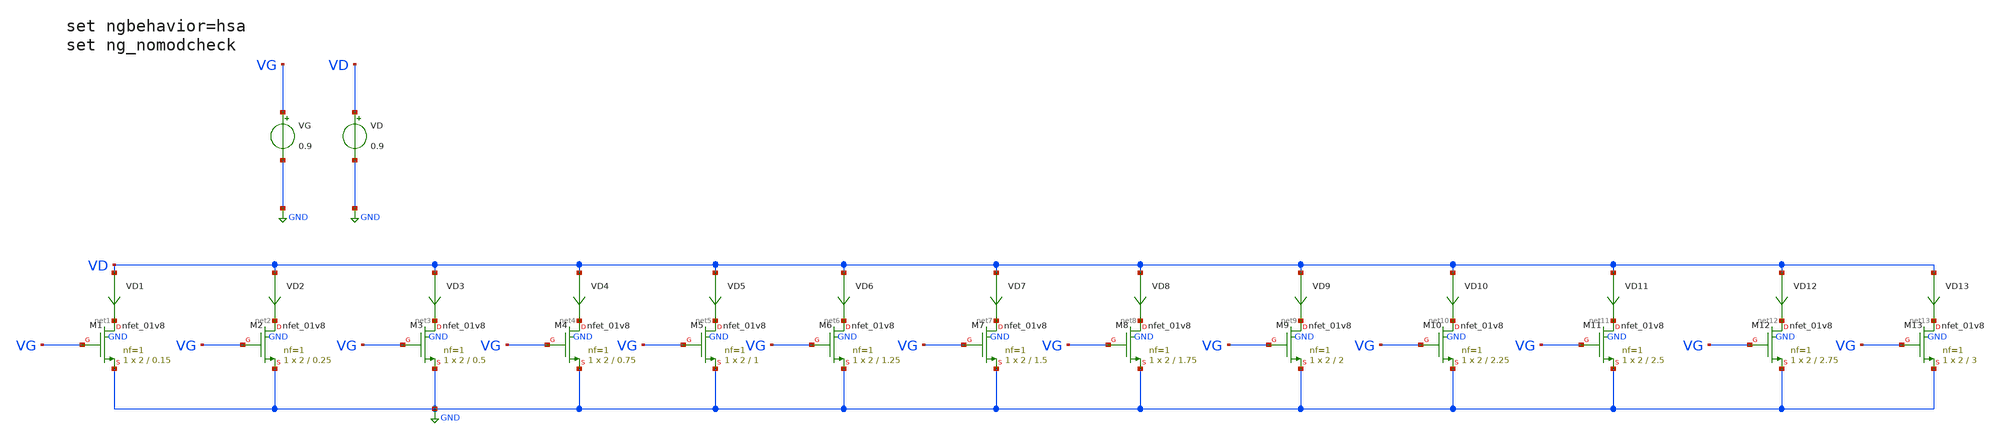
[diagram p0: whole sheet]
** sch_path: Design-Files/gmid_nmos_1v8_svt_tb.sch
**.subckt gmid_nmos_1v8_svt_tb
VG VG GND 0.9
VD VD GND 0.9
VD1 VD net1 0
.save i(vd1)
VD2 VD net2 0
.save i(vd2)
VD3 VD net3 0
.save i(vd3)
VD4 VD net4 0
.save i(vd4)
VD5 VD net5 0
.save i(vd5)
VD6 VD net6 0
.save i(vd6)
VD7 VD net7 0
.save i(vd7)
VD8 VD net8 0
.save i(vd8)
VD9 VD net9 0
.save i(vd9)
VD10 VD net10 0
.save i(vd10)
VD11 VD net11 0
.save i(vd11)
VD12 VD net12 0
.save i(vd12)
VD13 VD net13 0
.save i(vd13)
XM1 net1 VG GND GND sky130_fd_pr__nfet_01v8 L=0.15 W=2 nf=1 ad='int((nf+1)/2) * W/nf * 0.29' as='int((nf+2)/2) * W/nf * 0.29'
+ pd='2*int((nf+1)/2) * (W/nf + 0.29)' ps='2*int((nf+2)/2) * (W/nf + 0.29)' nrd='0.29 / W' nrs='0.29 / W'
+ sa=0 sb=0 sd=0 mult=1 m=1
XM2 net2 VG GND GND sky130_fd_pr__nfet_01v8 L=0.25 W=2 nf=1 ad='int((nf+1)/2) * W/nf * 0.29' as='int((nf+2)/2) * W/nf * 0.29'
+ pd='2*int((nf+1)/2) * (W/nf + 0.29)' ps='2*int((nf+2)/2) * (W/nf + 0.29)' nrd='0.29 / W' nrs='0.29 / W'
+ sa=0 sb=0 sd=0 mult=1 m=1
XM3 net3 VG GND GND sky130_fd_pr__nfet_01v8 L=0.5 W=2 nf=1 ad='int((nf+1)/2) * W/nf * 0.29' as='int((nf+2)/2) * W/nf * 0.29'
+ pd='2*int((nf+1)/2) * (W/nf + 0.29)' ps='2*int((nf+2)/2) * (W/nf + 0.29)' nrd='0.29 / W' nrs='0.29 / W'
+ sa=0 sb=0 sd=0 mult=1 m=1
XM4 net4 VG GND GND sky130_fd_pr__nfet_01v8 L=0.75 W=2 nf=1 ad='int((nf+1)/2) * W/nf * 0.29' as='int((nf+2)/2) * W/nf * 0.29'
+ pd='2*int((nf+1)/2) * (W/nf + 0.29)' ps='2*int((nf+2)/2) * (W/nf + 0.29)' nrd='0.29 / W' nrs='0.29 / W'
+ sa=0 sb=0 sd=0 mult=1 m=1
XM5 net5 VG GND GND sky130_fd_pr__nfet_01v8 L=1 W=2 nf=1 ad='int((nf+1)/2) * W/nf * 0.29' as='int((nf+2)/2) * W/nf * 0.29'
+ pd='2*int((nf+1)/2) * (W/nf + 0.29)' ps='2*int((nf+2)/2) * (W/nf + 0.29)' nrd='0.29 / W' nrs='0.29 / W'
+ sa=0 sb=0 sd=0 mult=1 m=1
XM6 net6 VG GND GND sky130_fd_pr__nfet_01v8 L=1.25 W=2 nf=1 ad='int((nf+1)/2) * W/nf * 0.29' as='int((nf+2)/2) * W/nf * 0.29'
+ pd='2*int((nf+1)/2) * (W/nf + 0.29)' ps='2*int((nf+2)/2) * (W/nf + 0.29)' nrd='0.29 / W' nrs='0.29 / W'
+ sa=0 sb=0 sd=0 mult=1 m=1
XM7 net7 VG GND GND sky130_fd_pr__nfet_01v8 L=1.5 W=2 nf=1 ad='int((nf+1)/2) * W/nf * 0.29' as='int((nf+2)/2) * W/nf * 0.29'
+ pd='2*int((nf+1)/2) * (W/nf + 0.29)' ps='2*int((nf+2)/2) * (W/nf + 0.29)' nrd='0.29 / W' nrs='0.29 / W'
+ sa=0 sb=0 sd=0 mult=1 m=1
XM8 net8 VG GND GND sky130_fd_pr__nfet_01v8 L=1.75 W=2 nf=1 ad='int((nf+1)/2) * W/nf * 0.29' as='int((nf+2)/2) * W/nf * 0.29'
+ pd='2*int((nf+1)/2) * (W/nf + 0.29)' ps='2*int((nf+2)/2) * (W/nf + 0.29)' nrd='0.29 / W' nrs='0.29 / W'
+ sa=0 sb=0 sd=0 mult=1 m=1
XM9 net9 VG GND GND sky130_fd_pr__nfet_01v8 L=2 W=2 nf=1 ad='int((nf+1)/2) * W/nf * 0.29' as='int((nf+2)/2) * W/nf * 0.29'
+ pd='2*int((nf+1)/2) * (W/nf + 0.29)' ps='2*int((nf+2)/2) * (W/nf + 0.29)' nrd='0.29 / W' nrs='0.29 / W'
+ sa=0 sb=0 sd=0 mult=1 m=1
XM10 net10 VG GND GND sky130_fd_pr__nfet_01v8 L=2.25 W=2 nf=1 ad='int((nf+1)/2) * W/nf * 0.29' as='int((nf+2)/2) * W/nf * 0.29'
+ pd='2*int((nf+1)/2) * (W/nf + 0.29)' ps='2*int((nf+2)/2) * (W/nf + 0.29)' nrd='0.29 / W' nrs='0.29 / W'
+ sa=0 sb=0 sd=0 mult=1 m=1
XM11 net11 VG GND GND sky130_fd_pr__nfet_01v8 L=2.5 W=2 nf=1 ad='int((nf+1)/2) * W/nf * 0.29' as='int((nf+2)/2) * W/nf * 0.29'
+ pd='2*int((nf+1)/2) * (W/nf + 0.29)' ps='2*int((nf+2)/2) * (W/nf + 0.29)' nrd='0.29 / W' nrs='0.29 / W'
+ sa=0 sb=0 sd=0 mult=1 m=1
XM12 net12 VG GND GND sky130_fd_pr__nfet_01v8 L=2.75 W=2 nf=1 ad='int((nf+1)/2) * W/nf * 0.29' as='int((nf+2)/2) * W/nf * 0.29'
+ pd='2*int((nf+1)/2) * (W/nf + 0.29)' ps='2*int((nf+2)/2) * (W/nf + 0.29)' nrd='0.29 / W' nrs='0.29 / W'
+ sa=0 sb=0 sd=0 mult=1 m=1
XM13 net13 VG GND GND sky130_fd_pr__nfet_01v8 L=3 W=2 nf=1 ad='int((nf+1)/2) * W/nf * 0.29' as='int((nf+2)/2) * W/nf * 0.29'
+ pd='2*int((nf+1)/2) * (W/nf + 0.29)' ps='2*int((nf+2)/2) * (W/nf + 0.29)' nrd='0.29 / W' nrs='0.29 / W'
+ sa=0 sb=0 sd=0 mult=1 m=1
**** begin user architecture code

** opencircuitdesign pdks install
.lib $::SKYWATER_MODELS/sky130.lib.spice ff



* ngspice commands
.option wnflag=1
.option savecurrents
.control
save all
save @m.xm1.msky130_fd_pr__nfet_01v8[gm]
save @m.xm1.msky130_fd_pr__nfet_01v8[vth]
save @m.xm1.msky130_fd_pr__nfet_01v8[gds]
save @m.xm1.msky130_fd_pr__nfet_01v8[cgg]
save @m.xm1.msky130_fd_pr__nfet_01v8[cgs]
save @m.xm1.msky130_fd_pr__nfet_01v8[cgd]
save @m.xm2.msky130_fd_pr__nfet_01v8[gm]
save @m.xm2.msky130_fd_pr__nfet_01v8[vth]
save @m.xm2.msky130_fd_pr__nfet_01v8[gds]
save @m.xm2.msky130_fd_pr__nfet_01v8[cgg]
save @m.xm2.msky130_fd_pr__nfet_01v8[cgs]
save @m.xm2.msky130_fd_pr__nfet_01v8[cgd]
save @m.xm3.msky130_fd_pr__nfet_01v8[gm]
save @m.xm3.msky130_fd_pr__nfet_01v8[vth]
save @m.xm3.msky130_fd_pr__nfet_01v8[gds]
save @m.xm3.msky130_fd_pr__nfet_01v8[cgg]
save @m.xm3.msky130_fd_pr__nfet_01v8[cgs]
save @m.xm3.msky130_fd_pr__nfet_01v8[cgd]
save @m.xm4.msky130_fd_pr__nfet_01v8[gm]
save @m.xm4.msky130_fd_pr__nfet_01v8[vth]
save @m.xm4.msky130_fd_pr__nfet_01v8[gds]
save @m.xm4.msky130_fd_pr__nfet_01v8[cgg]
save @m.xm4.msky130_fd_pr__nfet_01v8[cgs]
save @m.xm4.msky130_fd_pr__nfet_01v8[cgd]
save @m.xm5.msky130_fd_pr__nfet_01v8[gm]
save @m.xm5.msky130_fd_pr__nfet_01v8[vth]
save @m.xm5.msky130_fd_pr__nfet_01v8[gds]
save @m.xm5.msky130_fd_pr__nfet_01v8[cgg]
save @m.xm5.msky130_fd_pr__nfet_01v8[cgs]
save @m.xm5.msky130_fd_pr__nfet_01v8[cgd]
save @m.xm6.msky130_fd_pr__nfet_01v8[gm]
save @m.xm6.msky130_fd_pr__nfet_01v8[vth]
save @m.xm6.msky130_fd_pr__nfet_01v8[gds]
save @m.xm6.msky130_fd_pr__nfet_01v8[cgg]
save @m.xm6.msky130_fd_pr__nfet_01v8[cgs]
save @m.xm6.msky130_fd_pr__nfet_01v8[cgd]
save @m.xm7.msky130_fd_pr__nfet_01v8[gm]
save @m.xm7.msky130_fd_pr__nfet_01v8[vth]
save @m.xm7.msky130_fd_pr__nfet_01v8[gds]
save @m.xm7.msky130_fd_pr__nfet_01v8[cgg]
save @m.xm7.msky130_fd_pr__nfet_01v8[cgs]
save @m.xm7.msky130_fd_pr__nfet_01v8[cgd]
save @m.xm8.msky130_fd_pr__nfet_01v8[gm]
save @m.xm8.msky130_fd_pr__nfet_01v8[vth]
save @m.xm8.msky130_fd_pr__nfet_01v8[gds]
save @m.xm8.msky130_fd_pr__nfet_01v8[cgg]
save @m.xm8.msky130_fd_pr__nfet_01v8[cgs]
save @m.xm8.msky130_fd_pr__nfet_01v8[cgd]
save @m.xm9.msky130_fd_pr__nfet_01v8[gm]
save @m.xm9.msky130_fd_pr__nfet_01v8[vth]
save @m.xm9.msky130_fd_pr__nfet_01v8[gds]
save @m.xm9.msky130_fd_pr__nfet_01v8[cgg]
save @m.xm9.msky130_fd_pr__nfet_01v8[cgs]
save @m.xm9.msky130_fd_pr__nfet_01v8[cgd]
save @m.xm10.msky130_fd_pr__nfet_01v8[gm]
save @m.xm10.msky130_fd_pr__nfet_01v8[vth]
save @m.xm10.msky130_fd_pr__nfet_01v8[gds]
save @m.xm10.msky130_fd_pr__nfet_01v8[cgg]
save @m.xm10.msky130_fd_pr__nfet_01v8[cgs]
save @m.xm10.msky130_fd_pr__nfet_01v8[cgd]
save @m.xm11.msky130_fd_pr__nfet_01v8[gm]
save @m.xm11.msky130_fd_pr__nfet_01v8[vth]
save @m.xm11.msky130_fd_pr__nfet_01v8[gds]
save @m.xm11.msky130_fd_pr__nfet_01v8[cgg]
save @m.xm11.msky130_fd_pr__nfet_01v8[cgs]
save @m.xm11.msky130_fd_pr__nfet_01v8[cgd]
save @m.xm12.msky130_fd_pr__nfet_01v8[gm]
save @m.xm12.msky130_fd_pr__nfet_01v8[vth]
save @m.xm12.msky130_fd_pr__nfet_01v8[gds]
save @m.xm12.msky130_fd_pr__nfet_01v8[cgg]
save @m.xm12.msky130_fd_pr__nfet_01v8[cgs]
save @m.xm12.msky130_fd_pr__nfet_01v8[cgd]
save @m.xm13.msky130_fd_pr__nfet_01v8[gm]
save @m.xm13.msky130_fd_pr__nfet_01v8[vth]
save @m.xm13.msky130_fd_pr__nfet_01v8[gds]
save @m.xm13.msky130_fd_pr__nfet_01v8[cgg]
save @m.xm13.msky130_fd_pr__nfet_01v8[cgs]
save @m.xm13.msky130_fd_pr__nfet_01v8[cgd]
dc VG 0.05 1.8 0.1m
** remove zero length vectors to prevent write errors
remzerovec
write /foss/designs/PDKCHAR/gmid_nmos_svt_tb.raw

plot @m.xm1.msky130_fd_pr__nfet_01v8[gm]
plot @m.xm2.msky130_fd_pr__nfet_01v8[gm]
plot @m.xm3.msky130_fd_pr__nfet_01v8[gm]
plot @m.xm4.msky130_fd_pr__nfet_01v8[gm]
plot @m.xm5.msky130_fd_pr__nfet_01v8[gm]
plot @m.xm6.msky130_fd_pr__nfet_01v8[gm]
plot @m.xm7.msky130_fd_pr__nfet_01v8[gm]
plot @m.xm8.msky130_fd_pr__nfet_01v8[gm]
plot @m.xm9.msky130_fd_pr__nfet_01v8[gm]
plot @m.xm10.msky130_fd_pr__nfet_01v8[gm]
plot @m.xm11.msky130_fd_pr__nfet_01v8[gm]
plot @m.xm12.msky130_fd_pr__nfet_01v8[gm]
plot @m.xm13.msky130_fd_pr__nfet_01v8[gm]

wrdata /foss/designs/PDKCHAR/gmid_nmos_1_nfet_01v8_svt_tb.txt @m.xm1.msky130_fd_pr__nfet_01v8[gm]
+ i(VD1) @m.xm1.msky130_fd_pr__nfet_01v8[vth] @m.xm1.msky130_fd_pr__nfet_01v8[gds]
+ @m.xm1.msky130_fd_pr__nfet_01v8[cgg] @m.xm1.msky130_fd_pr__nfet_01v8[cgs] @m.xm1.msky130_fd_pr__nfet_01v8[cgd]
wrdata /foss/designs/PDKCHAR/gmid_nmos_2_nfet_01v8_svt_tb.txt @m.xm2.msky130_fd_pr__nfet_01v8[gm]
+ i(VD2) @m.xm2.msky130_fd_pr__nfet_01v8[vth] @m.xm2.msky130_fd_pr__nfet_01v8[gds]
+ @m.xm2.msky130_fd_pr__nfet_01v8[cgg] @m.xm2.msky130_fd_pr__nfet_01v8[cgs] @m.xm2.msky130_fd_pr__nfet_01v8[cgd]
wrdata /foss/designs/PDKCHAR/gmid_nmos_3_nfet_01v8_svt_tb.txt @m.xm3.msky130_fd_pr__nfet_01v8[gm]
+ i(VD3) @m.xm3.msky130_fd_pr__nfet_01v8[vth] @m.xm3.msky130_fd_pr__nfet_01v8[gds]
+ @m.xm3.msky130_fd_pr__nfet_01v8[cgg] @m.xm3.msky130_fd_pr__nfet_01v8[cgs] @m.xm3.msky130_fd_pr__nfet_01v8[cgd]
wrdata /foss/designs/PDKCHAR/gmid_nmos_4_nfet_01v8_svt_tb.txt @m.xm4.msky130_fd_pr__nfet_01v8[gm]
+ i(VD4) @m.xm4.msky130_fd_pr__nfet_01v8[vth] @m.xm4.msky130_fd_pr__nfet_01v8[gds]
+ @m.xm4.msky130_fd_pr__nfet_01v8[cgg] @m.xm4.msky130_fd_pr__nfet_01v8[cgs] @m.xm4.msky130_fd_pr__nfet_01v8[cgd]
wrdata /foss/designs/PDKCHAR/gmid_nmos_5_nfet_01v8_svt_tb.txt @m.xm5.msky130_fd_pr__nfet_01v8[gm]
+ i(VD5) @m.xm5.msky130_fd_pr__nfet_01v8[vth] @m.xm5.msky130_fd_pr__nfet_01v8[gds]
+ @m.xm5.msky130_fd_pr__nfet_01v8[cgg] @m.xm5.msky130_fd_pr__nfet_01v8[cgs] @m.xm5.msky130_fd_pr__nfet_01v8[cgd]
wrdata /foss/designs/PDKCHAR/gmid_nmos_6_nfet_01v8_svt_tb.txt @m.xm6.msky130_fd_pr__nfet_01v8[gm]
+ i(VD6) @m.xm6.msky130_fd_pr__nfet_01v8[vth] @m.xm6.msky130_fd_pr__nfet_01v8[gds]
+ @m.xm6.msky130_fd_pr__nfet_01v8[cgg] @m.xm6.msky130_fd_pr__nfet_01v8[cgs] @m.xm6.msky130_fd_pr__nfet_01v8[cgd]
wrdata /foss/designs/PDKCHAR/gmid_nmos_7_nfet_01v8_svt_tb.txt @m.xm7.msky130_fd_pr__nfet_01v8[gm]
+ i(VD7) @m.xm7.msky130_fd_pr__nfet_01v8[vth] @m.xm7.msky130_fd_pr__nfet_01v8[gds]
+ @m.xm7.msky130_fd_pr__nfet_01v8[cgg] @m.xm7.msky130_fd_pr__nfet_01v8[cgs] @m.xm7.msky130_fd_pr__nfet_01v8[cgd]
wrdata /foss/designs/PDKCHAR/gmid_nmos_8_nfet_01v8_svt_tb.txt @m.xm8.msky130_fd_pr__nfet_01v8[gm]
+ i(VD8) @m.xm8.msky130_fd_pr__nfet_01v8[vth] @m.xm8.msky130_fd_pr__nfet_01v8[gds]
+ @m.xm8.msky130_fd_pr__nfet_01v8[cgg] @m.xm8.msky130_fd_pr__nfet_01v8[cgs] @m.xm8.msky130_fd_pr__nfet_01v8[cgd]
wrdata /foss/designs/PDKCHAR/gmid_nmos_9_nfet_01v8_svt_tb.txt @m.xm9.msky130_fd_pr__nfet_01v8[gm]
+ i(VD9) @m.xm9.msky130_fd_pr__nfet_01v8[vth] @m.xm9.msky130_fd_pr__nfet_01v8[gds]
+ @m.xm9.msky130_fd_pr__nfet_01v8[cgg] @m.xm9.msky130_fd_pr__nfet_01v8[cgs] @m.xm9.msky130_fd_pr__nfet_01v8[cgd]
wrdata /foss/designs/PDKCHAR/gmid_nmos_10_nfet_01v8_svt_tb.txt @m.xm10.msky130_fd_pr__nfet_01v8[gm]
+ i(VD10) @m.xm10.msky130_fd_pr__nfet_01v8[vth] @m.xm10.msky130_fd_pr__nfet_01v8[gds]
+ @m.xm10.msky130_fd_pr__nfet_01v8[cgg] @m.xm10.msky130_fd_pr__nfet_01v8[cgs] @m.xm10.msky130_fd_pr__nfet_01v8[cgd]
wrdata /foss/designs/PDKCHAR/gmid_nmos_11_nfet_01v8_svt_tb.txt @m.xm11.msky130_fd_pr__nfet_01v8[gm]
+ i(VD11) @m.xm11.msky130_fd_pr__nfet_01v8[vth] @m.xm11.msky130_fd_pr__nfet_01v8[gds]
+ @m.xm11.msky130_fd_pr__nfet_01v8[cgg] @m.xm11.msky130_fd_pr__nfet_01v8[cgs] @m.xm11.msky130_fd_pr__nfet_01v8[cgd]
wrdata /foss/designs/PDKCHAR/gmid_nmos_12_nfet_01v8_svt_tb.txt @m.xm12.msky130_fd_pr__nfet_01v8[gm]
+ i(VD12) @m.xm12.msky130_fd_pr__nfet_01v8[vth] @m.xm12.msky130_fd_pr__nfet_01v8[gds]
+ @m.xm12.msky130_fd_pr__nfet_01v8[cgg] @m.xm12.msky130_fd_pr__nfet_01v8[cgs] @m.xm12.msky130_fd_pr__nfet_01v8[cgd]
wrdata /foss/designs/PDKCHAR/gmid_nmos_13_nfet_01v8_svt_tb.txt @m.xm13.msky130_fd_pr__nfet_01v8[gm]
+ i(VD13) @m.xm13.msky130_fd_pr__nfet_01v8[vth] @m.xm13.msky130_fd_pr__nfet_01v8[gds]
+ @m.xm13.msky130_fd_pr__nfet_01v8[cgg] @m.xm13.msky130_fd_pr__nfet_01v8[cgs] @m.xm13.msky130_fd_pr__nfet_01v8[cgd]
set appendwrite
op
remzerovec
write /foss/designs/PDKCHAR/gmid_nmos_svt_tb.raw
**quit 0
.endc


**** end user architecture code
**.ends
.GLOBAL GND
.end
